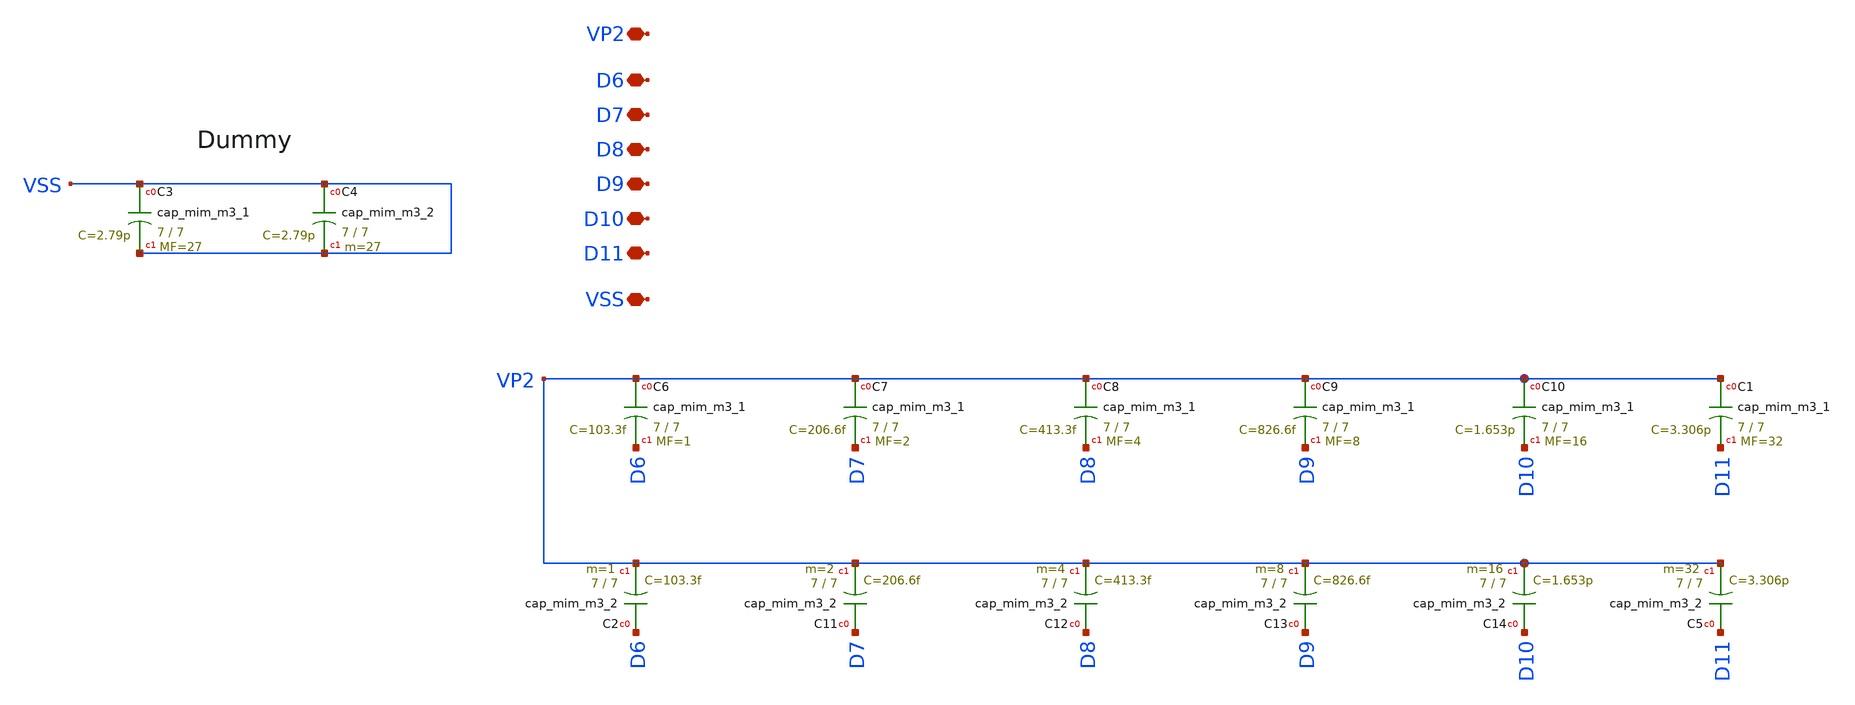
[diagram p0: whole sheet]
** sch_path: xschem/EF_MSB_CAP.sch
**.subckt EF_MSB_CAP D10 D6 D7 D8 D9 VP2 VSS D11
*.iopin D10
*.iopin D6
*.iopin D7
*.iopin D8
*.iopin D9
*.iopin VP2
*.iopin VSS
*.iopin D11
XC2 D6 VP2 sky130_fd_pr__cap_mim_m3_2 W=7 L=7 MF=1 m=1
XC3 VSS VSS sky130_fd_pr__cap_mim_m3_1 W=7 L=7 MF=27 m=27
XC4 VSS VSS sky130_fd_pr__cap_mim_m3_2 W=7 L=7 MF=27 m=27
XC6 VP2 D6 sky130_fd_pr__cap_mim_m3_1 W=7 L=7 MF=1 m=1
XC7 VP2 D7 sky130_fd_pr__cap_mim_m3_1 W=7 L=7 MF=2 m=2
XC8 VP2 D8 sky130_fd_pr__cap_mim_m3_1 W=7 L=7 MF=4 m=4
XC9 VP2 D9 sky130_fd_pr__cap_mim_m3_1 W=7 L=7 MF=8 m=8
XC10 VP2 D10 sky130_fd_pr__cap_mim_m3_1 W=7 L=7 MF=16 m=16
XC11 D7 VP2 sky130_fd_pr__cap_mim_m3_2 W=7 L=7 MF=2 m=2
XC12 D8 VP2 sky130_fd_pr__cap_mim_m3_2 W=7 L=7 MF=4 m=4
XC13 D9 VP2 sky130_fd_pr__cap_mim_m3_2 W=7 L=7 MF=8 m=8
XC14 D10 VP2 sky130_fd_pr__cap_mim_m3_2 W=7 L=7 MF=16 m=16
XC1 VP2 D11 sky130_fd_pr__cap_mim_m3_1 W=7 L=7 MF=32 m=32
XC5 D11 VP2 sky130_fd_pr__cap_mim_m3_2 W=7 L=7 MF=32 m=32
**.ends
.end
